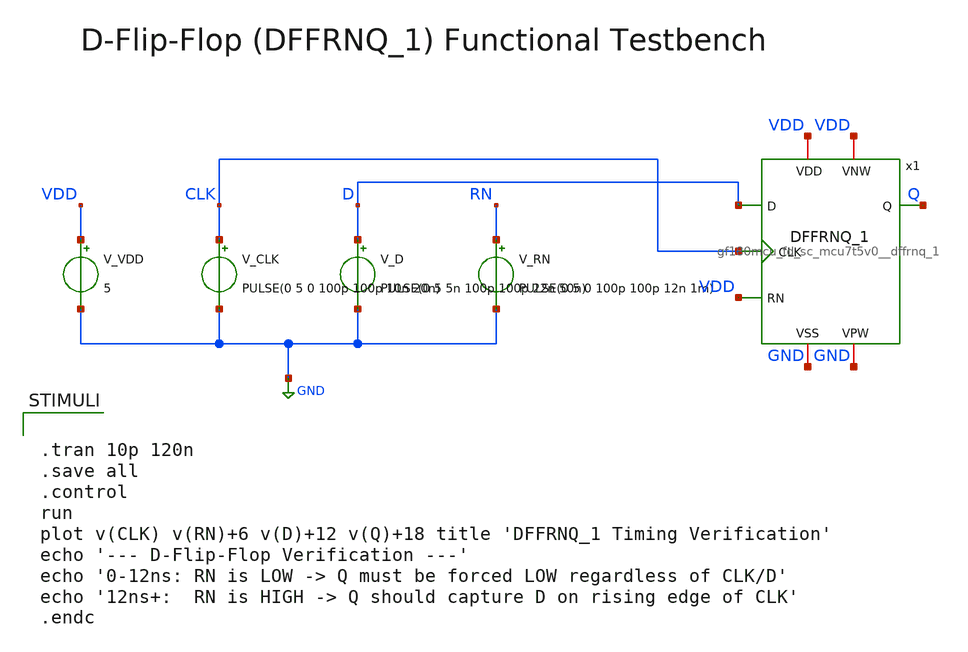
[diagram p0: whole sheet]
** sch_path: designs/libs/core_analog/pfd/DFF_tb.sch
**.subckt DFF_tb
V_VDD VDD GND 5
V_CLK CLK GND PULSE(0 5 0 100p 100p 10n 20n)
V_D D GND PULSE(0 5 5n 100p 100p 22n 50n)
V_RN RN GND PULSE(0 5 0 100p 100p 12n 1m)
x1 D VDD CLK Q VDD VDD GND GND gf180mcu_fd_sc_mcu7t5v0__dffrnq_1
**** begin user architecture code


.tran 10p 120n
.save all
.control
run
plot v(CLK) v(RN)+6 v(D)+12 v(Q)+18 title 'DFFRNQ_1 Timing Verification'
echo '--- D-Flip-Flop Verification ---'
echo '0-12ns: RN is LOW -> Q must be forced LOW regardless of CLK/D'
echo '12ns+:  RN is HIGH -> Q should capture D on rising edge of CLK'
.endc



.include /foss/pdks/ciel/gf180mcu/versions/7b70722e33c03fcb5dabcf4d479fb0822d9251c9/gf180mcuD/libs.ref/gf180mcu_fd_sc_mcu7t5v0/spice/gf180mcu_fd_sc_mcu7t5v0.spice
.include $::180MCU_MODELS/design.ngspice
.lib $::180MCU_MODELS/sm141064.ngspice typical


**** end user architecture code
**.ends
.GLOBAL GND
.end
